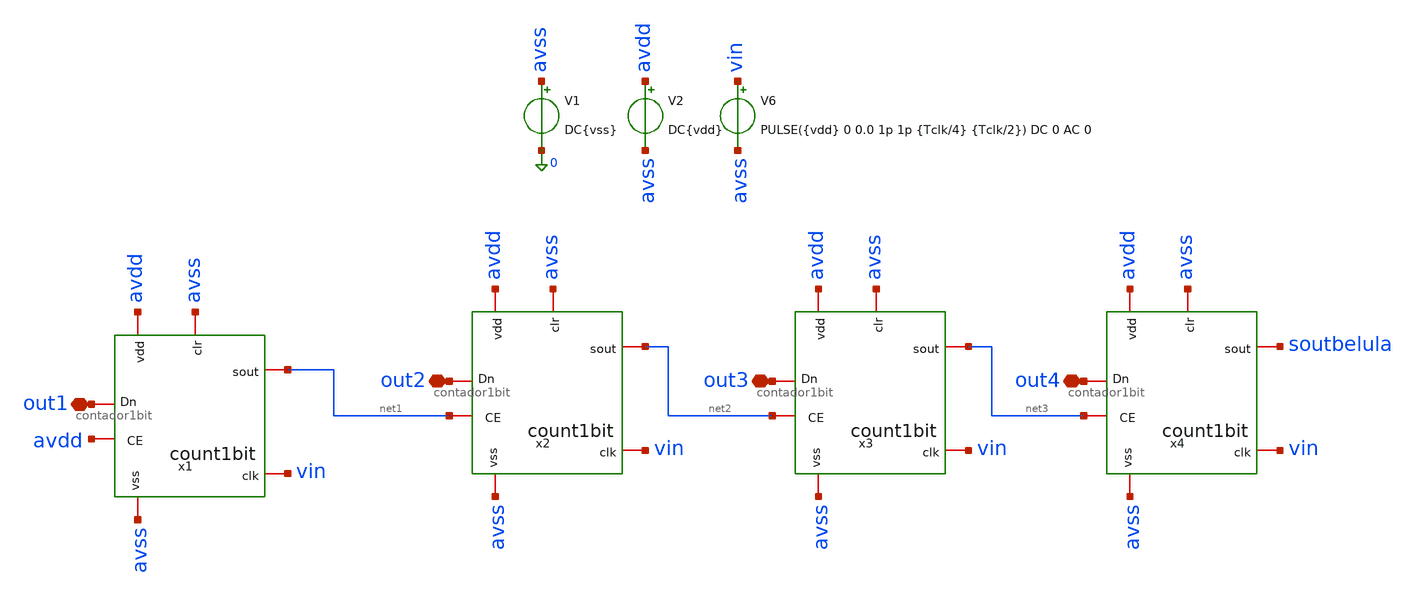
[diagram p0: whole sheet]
** sch_path: verification/testbenches/countador1bit/contador1bit.sch
**.subckt contador1bit out1 out2 out3 out4
*.iopin out1
*.iopin out2
*.iopin out3
*.iopin out4
x1 avss out1 avdd vin avdd avss net1 contador1bit
V1 avss 0 DC{vss}
V2 avdd avss DC{vdd}
V6 vin avss PULSE({vdd} 0 0.0 1p 1p {Tclk/4} {Tclk/2}) DC 0 AC 0
x2 avss out2 net1 vin avdd avss net2 contador1bit
x3 avss out3 net2 vin avdd avss net3 contador1bit
x4 avss out4 net3 vin avdd avss soutbelula contador1bit
**** begin user architecture code


* Circuit Parameters
.param vdd = 1.2
.param vss = 0.0
.param Tclk = 10n
.options TEMP = 27.0
* Include Models - IHP SG13G2
.lib cornerMOSlv.lib mos_tt
* OP Parameters & Singals to save
.save all
*Simulations
.control
tran 0.01u 100n
setplot tran1
plot v(vin) v(out1)+1.2 v(out2)+2.4 v(out3)+3.6 v(out4)+4.8
reset
dc V6 0 1.2 0.01
setplot dc
set filetype = ascii
write dcsweep.raw
.endc
.end


**** end user architecture code
**.ends
.end
